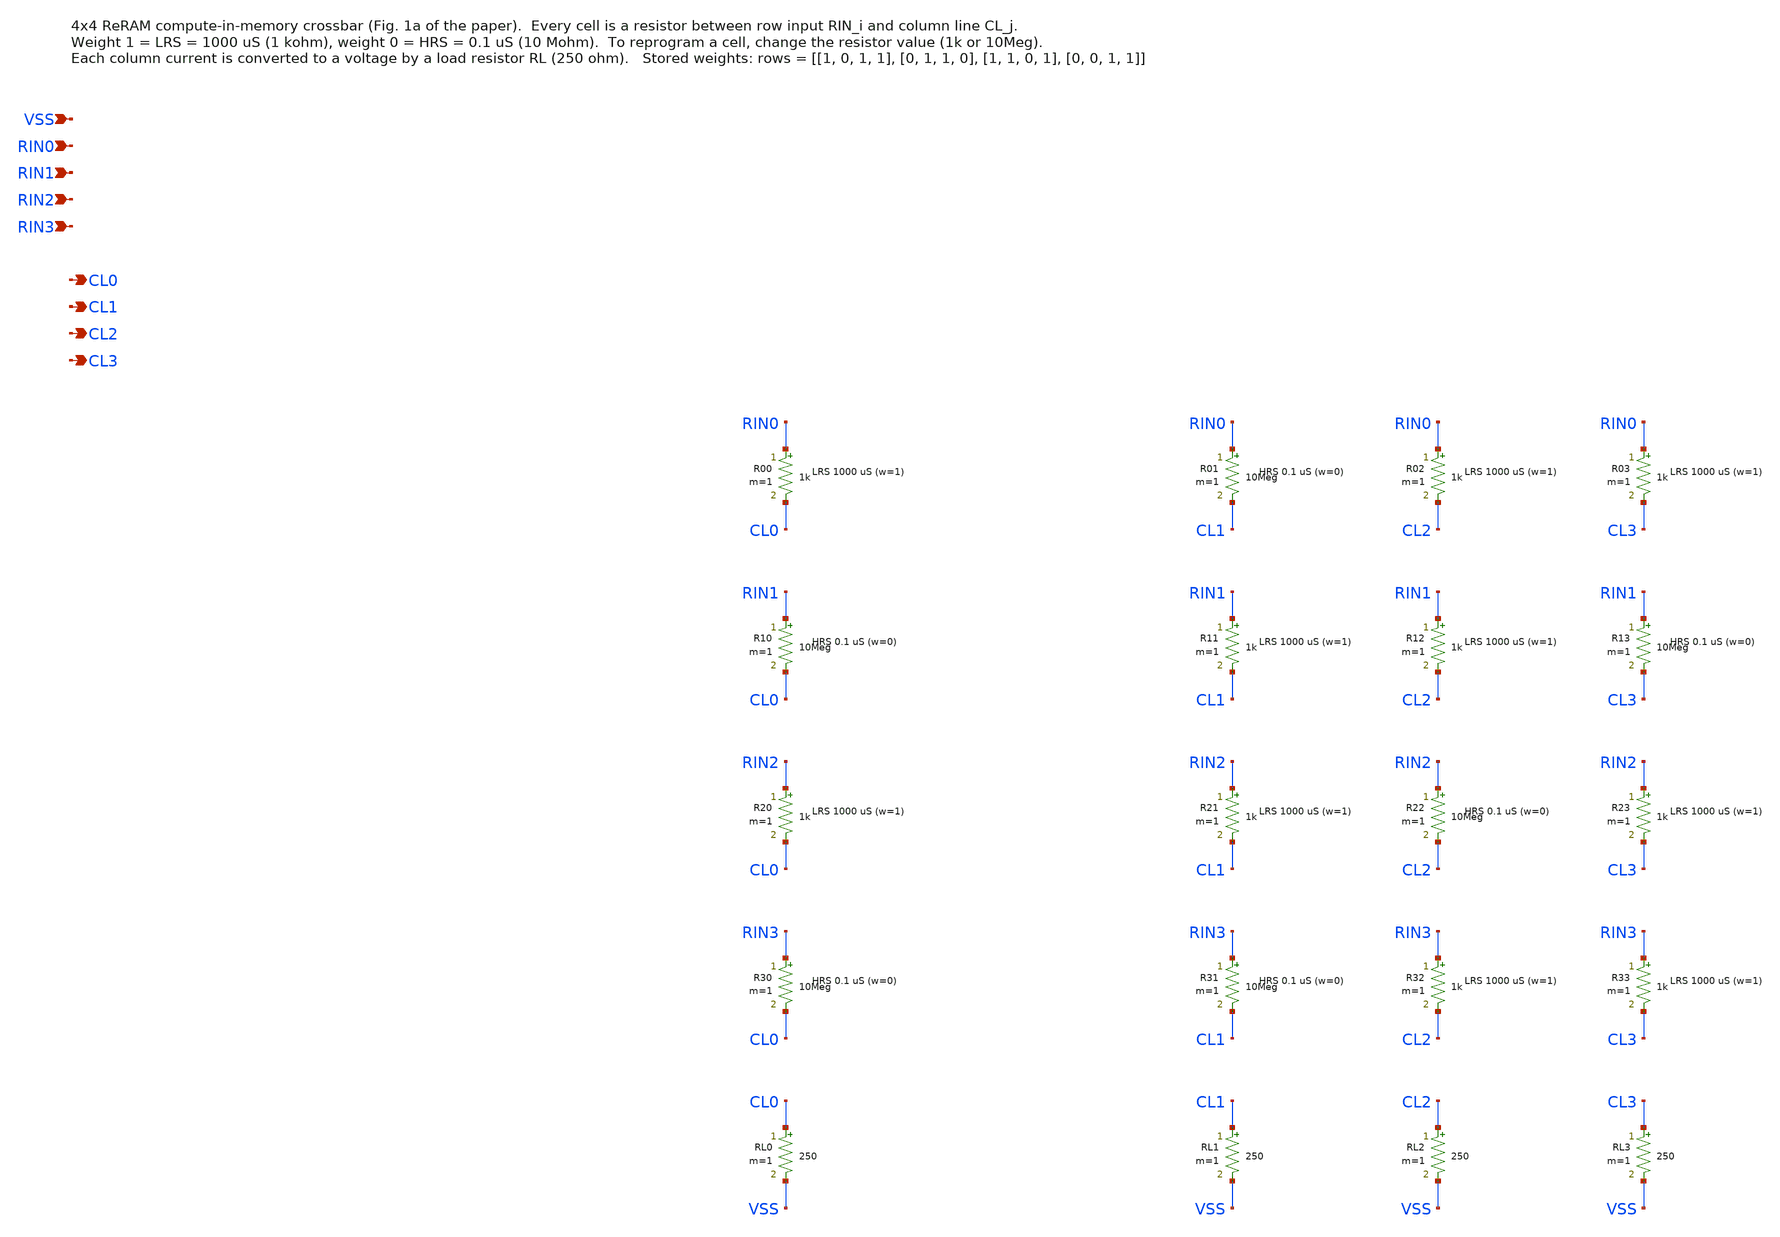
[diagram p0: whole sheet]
** sch_path: CiM components/cim_reram_4x4.sch
**.subckt cim_reram_4x4 VSS RIN0 RIN1 RIN2 RIN3 CL0 CL1 CL2 CL3
*.ipin VSS
*.ipin RIN0
*.ipin RIN1
*.ipin RIN2
*.ipin RIN3
*.opin CL0
*.opin CL1
*.opin CL2
*.opin CL3
R00 RIN0 CL0 1k m=1
R01 RIN0 CL1 10Meg m=1
R02 RIN0 CL2 1k m=1
R03 RIN0 CL3 1k m=1
R10 RIN1 CL0 10Meg m=1
R11 RIN1 CL1 1k m=1
R12 RIN1 CL2 1k m=1
R13 RIN1 CL3 10Meg m=1
R20 RIN2 CL0 1k m=1
R21 RIN2 CL1 1k m=1
R22 RIN2 CL2 10Meg m=1
R23 RIN2 CL3 1k m=1
R30 RIN3 CL0 10Meg m=1
R31 RIN3 CL1 10Meg m=1
R32 RIN3 CL2 1k m=1
R33 RIN3 CL3 1k m=1
RL0 CL0 VSS 250 m=1
RL1 CL1 VSS 250 m=1
RL2 CL2 VSS 250 m=1
RL3 CL3 VSS 250 m=1
**.ends
.end
